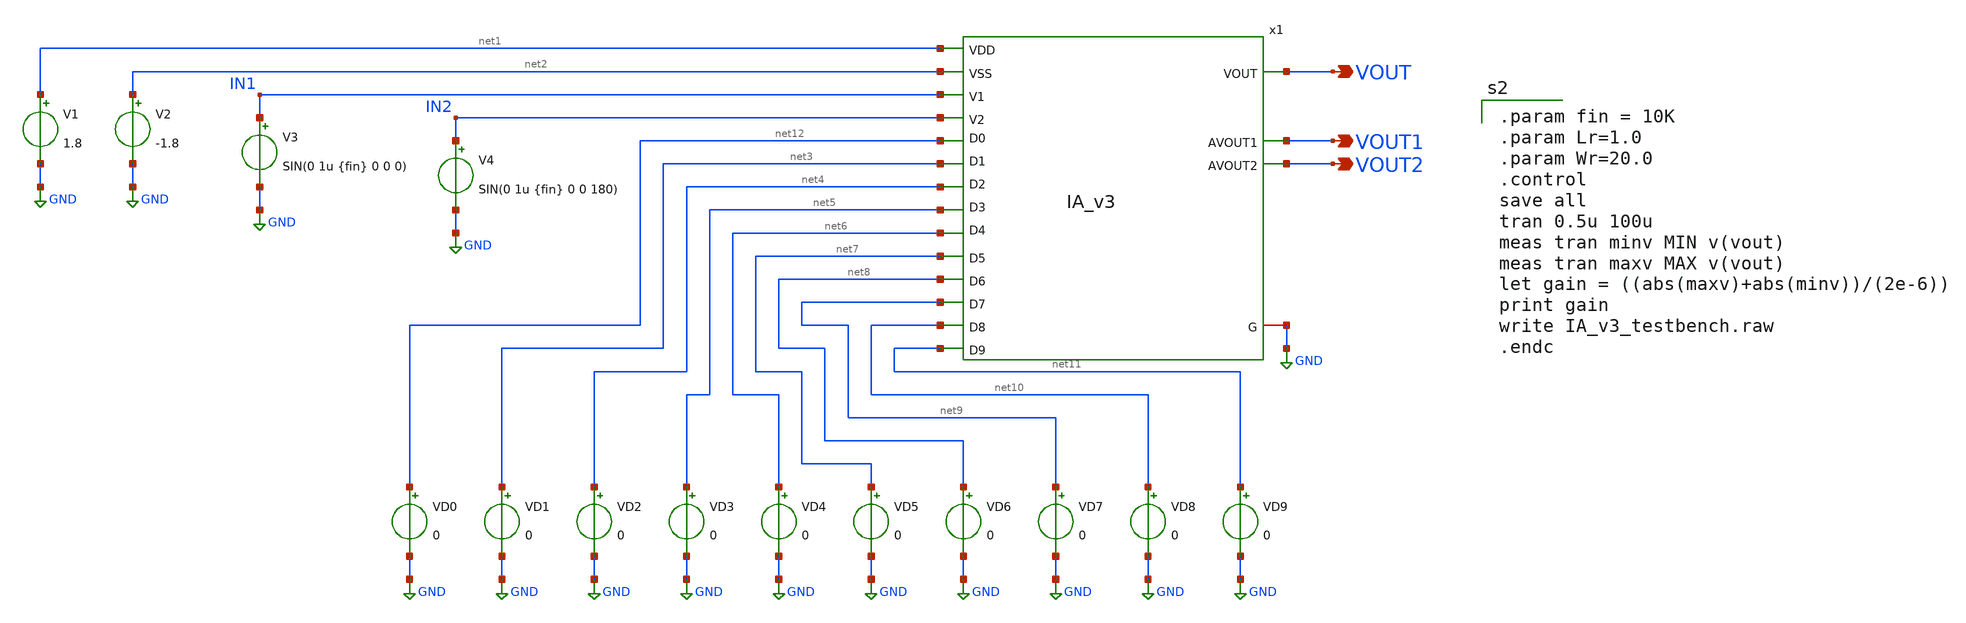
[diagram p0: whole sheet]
** sch_path: xschem/IA_v3_testbench.sch
**.subckt IA_v3_testbench VOUT VOUT1 VOUT2
*.opin VOUT
*.opin VOUT1
*.opin VOUT2
V1 net1 GND 1.8
V2 net2 GND -1.8
V3 IN1 GND SIN(0 1u {fin} 0 0 0)
V4 IN2 GND SIN(0 1u {fin} 0 0 180)
VD0 net12 GND 0
VD1 net3 GND 0
VD2 net4 GND 0
VD3 net5 GND 0
VD4 net6 GND 0
VD5 net7 GND 0
VD6 net8 GND 0
VD7 net9 GND 0
VD8 net10 GND 0
VD9 net11 GND 0
x1 VOUT1 net1 net2 VOUT IN1 IN2 VOUT2 net6 net5 net4 net3 net12 GND net8 net9 net10 net7 net11 IA_v3
**** begin user architecture code

.param fin = 10K
.param Lr=1.0
.param Wr=20.0
.control
save all
tran 0.5u 100u
meas tran minv MIN v(vout)
meas tran maxv MAX v(vout)
let gain = ((abs(maxv)+abs(minv))/(2e-6))
print gain
write IA_v3_testbench.raw
.endc

.lib $::SKYWATER_MODELS/sky130.lib.spice tt
**** end user architecture code
**.ends

* expanding   symbol:  ./IA_v3.sym # of pins=18
** sym_path: xschem/IA_v3.sym
** sch_path: xschem/IA_v3.sch
.subckt IA_v3 AVOUT1 VDD VSS VOUT V1 V2 AVOUT2 D4 D3 D2 D1 D0 G D6 D7 D8 D5 D9
*.opin VOUT
*.iopin G
*.ipin VDD
*.ipin VSS
*.ipin V1
*.ipin V2
*.ipin D4
*.ipin D3
*.ipin D2
*.ipin D1
*.ipin D0
*.ipin D9
*.ipin D8
*.ipin D7
*.ipin D6
*.ipin D5
*.opin AVOUT1
*.opin AVOUT2
x4 VDD VSS V2 net3 AVOUT1 opamp
x5 VDD VSS V1 net4 AVOUT2 opamp
x6 VDD VSS net2 net1 VOUT opamp
x1 G net3 AVOUT1 D0 D1 D2 D3 D4 VDD RA_array_v2
x2 G net4 AVOUT2 D0 D1 D2 D3 D4 VDD RA_array_v2
x3 G net1 VOUT D5 D6 D7 D8 D9 VDD RA_array_v2
x7 G net2 G D5 D6 D7 D8 D9 VDD RA_array_v2
XR1 net4 net3 G sky130_fd_pr__res_high_po_0p69 L=12.22 mult=64 m=64
XR2 net1 net6 G sky130_fd_pr__res_high_po_0p69 L=12.22 mult=64 m=64
XR3 net5 net2 G sky130_fd_pr__res_high_po_0p69 L=12.22 mult=64 m=64
x8 VDD VSS AVOUT2 net5 net5 opamp
x9 VDD VSS AVOUT1 net6 net6 opamp
.ends


* expanding   symbol:  ../xschem/opamp.sym # of pins=5
** sym_path: xschem/opamp.sym
** sch_path: xschem/opamp.sch
.subckt opamp VDD VSS V1 V2 VOUT
*.ipin VSS
*.ipin VDD
*.ipin V2
*.ipin V1
*.opin VOUT
XM2 net5 V2 net1 VSS sky130_fd_pr__nfet_01v8 L=1 W=8.5 nf=1 ad='int((nf+1)/2) * W/nf * 0.29' as='int((nf+2)/2) * W/nf * 0.29'
+ pd='2*int((nf+1)/2) * (W/nf + 0.29)' ps='2*int((nf+2)/2) * (W/nf + 0.29)' nrd='0.29 / W' nrs='0.29 / W'
+ sa=0 sb=0 sd=0 mult=1 m=1
XM1 net6 net5 VDD VDD sky130_fd_pr__pfet_01v8 L=1 W=41 nf=1 ad='int((nf+1)/2) * W/nf * 0.29' as='int((nf+2)/2) * W/nf * 0.29'
+ pd='2*int((nf+1)/2) * (W/nf + 0.29)' ps='2*int((nf+2)/2) * (W/nf + 0.29)' nrd='0.29 / W' nrs='0.29 / W'
+ sa=0 sb=0 sd=0 mult=1 m=1
XM4 net6 V1 net1 VSS sky130_fd_pr__nfet_01v8 L=1 W=8.5 nf=1 ad='int((nf+1)/2) * W/nf * 0.29' as='int((nf+2)/2) * W/nf * 0.29'
+ pd='2*int((nf+1)/2) * (W/nf + 0.29)' ps='2*int((nf+2)/2) * (W/nf + 0.29)' nrd='0.29 / W' nrs='0.29 / W'
+ sa=0 sb=0 sd=0 mult=1 m=1
XM5 net1 net4 VSS VSS sky130_fd_pr__nfet_01v8 L=1 W=20 nf=1 ad='int((nf+1)/2) * W/nf * 0.29' as='int((nf+2)/2) * W/nf * 0.29'
+ pd='2*int((nf+1)/2) * (W/nf + 0.29)' ps='2*int((nf+2)/2) * (W/nf + 0.29)' nrd='0.29 / W' nrs='0.29 / W'
+ sa=0 sb=0 sd=0 mult=1 m=1
XM6 VOUT net4 VSS VSS sky130_fd_pr__nfet_01v8 L=1 W=19 nf=1 ad='int((nf+1)/2) * W/nf * 0.29' as='int((nf+2)/2) * W/nf * 0.29'
+ pd='2*int((nf+1)/2) * (W/nf + 0.29)' ps='2*int((nf+2)/2) * (W/nf + 0.29)' nrd='0.29 / W' nrs='0.29 / W'
+ sa=0 sb=0 sd=0 mult=1 m=1
XM7 net4 net4 VSS VSS sky130_fd_pr__nfet_01v8 L=1 W=20 nf=1 ad='int((nf+1)/2) * W/nf * 0.29' as='int((nf+2)/2) * W/nf * 0.29'
+ pd='2*int((nf+1)/2) * (W/nf + 0.29)' ps='2*int((nf+2)/2) * (W/nf + 0.29)' nrd='0.29 / W' nrs='0.29 / W'
+ sa=0 sb=0 sd=0 mult=1 m=1
XM3 net5 net5 VDD VDD sky130_fd_pr__pfet_01v8 L=1 W=41 nf=1 ad='int((nf+1)/2) * W/nf * 0.29' as='int((nf+2)/2) * W/nf * 0.29'
+ pd='2*int((nf+1)/2) * (W/nf + 0.29)' ps='2*int((nf+2)/2) * (W/nf + 0.29)' nrd='0.29 / W' nrs='0.29 / W'
+ sa=0 sb=0 sd=0 mult=1 m=1
XM8 VOUT net6 VDD VDD sky130_fd_pr__pfet_01v8 L=1 W=40 nf=1 ad='int((nf+1)/2) * W/nf * 0.29' as='int((nf+2)/2) * W/nf * 0.29'
+ pd='2*int((nf+1)/2) * (W/nf + 0.29)' ps='2*int((nf+2)/2) * (W/nf + 0.29)' nrd='0.29 / W' nrs='0.29 / W'
+ sa=0 sb=0 sd=0 mult=2 m=2
XR3 net2 VDD VSS sky130_fd_pr__res_high_po W=1 L=50 mult=1 m=1
XR1 net3 net2 VSS sky130_fd_pr__res_high_po W=1 L=50 mult=1 m=1
XR2 net4 net3 VSS sky130_fd_pr__res_high_po W=1 L=50 mult=1 m=1
XR4 net7 VOUT VSS sky130_fd_pr__res_high_po W=1 L=7 mult=1 m=1
XC1 net7 net6 sky130_fd_pr__cap_mim_m3_1 W=5.55 L=10 MF=20 m=20
.ends


* expanding   symbol:  ../xschem/RA_array_v2.sym # of pins=9
** sym_path: xschem/RA_array_v2.sym
** sch_path: xschem/RA_array_v2.sch
.subckt RA_array_v2 VSS R1 R2 D0 D1 D2 D3 D4 VDD
*.ipin VSS
*.iopin R2
*.ipin D0
*.ipin D1
*.ipin D2
*.ipin D3
*.ipin D4
*.iopin R1
*.ipin VDD
XM1 net7 VDD net1 VSS sky130_fd_pr__nfet_g5v0d10v5 L={Lr} W={Wr} nf=1 ad='int((nf+1)/2) * W/nf * 0.29'
+ as='int((nf+2)/2) * W/nf * 0.29' pd='2*int((nf+1)/2) * (W/nf + 0.29)' ps='2*int((nf+2)/2) * (W/nf + 0.29)'
+ nrd='0.29 / W' nrs='0.29 / W' sa=0 sb=0 sd=0 mult=1 m=1
XM2 net8 D0 net2 VSS sky130_fd_pr__nfet_g5v0d10v5 L={Lr} W={Wr} nf=1 ad='int((nf+1)/2) * W/nf * 0.29'
+ as='int((nf+2)/2) * W/nf * 0.29' pd='2*int((nf+1)/2) * (W/nf + 0.29)' ps='2*int((nf+2)/2) * (W/nf + 0.29)'
+ nrd='0.29 / W' nrs='0.29 / W' sa=0 sb=0 sd=0 mult=1 m=1
XM3 net9 D1 net3 VSS sky130_fd_pr__nfet_g5v0d10v5 L={Lr} W={Wr} nf=1 ad='int((nf+1)/2) * W/nf * 0.29'
+ as='int((nf+2)/2) * W/nf * 0.29' pd='2*int((nf+1)/2) * (W/nf + 0.29)' ps='2*int((nf+2)/2) * (W/nf + 0.29)'
+ nrd='0.29 / W' nrs='0.29 / W' sa=0 sb=0 sd=0 mult=1 m=1
XM4 net10 D2 net4 VSS sky130_fd_pr__nfet_g5v0d10v5 L={Lr} W={Wr} nf=1 ad='int((nf+1)/2) * W/nf * 0.29'
+ as='int((nf+2)/2) * W/nf * 0.29' pd='2*int((nf+1)/2) * (W/nf + 0.29)' ps='2*int((nf+2)/2) * (W/nf + 0.29)'
+ nrd='0.29 / W' nrs='0.29 / W' sa=0 sb=0 sd=0 mult=1 m=1
XM5 net11 D3 net5 VSS sky130_fd_pr__nfet_g5v0d10v5 L={Lr} W={Wr} nf=1 ad='int((nf+1)/2) * W/nf * 0.29'
+ as='int((nf+2)/2) * W/nf * 0.29' pd='2*int((nf+1)/2) * (W/nf + 0.29)' ps='2*int((nf+2)/2) * (W/nf + 0.29)'
+ nrd='0.29 / W' nrs='0.29 / W' sa=0 sb=0 sd=0 mult=1 m=1
XM6 net12 D4 net6 VSS sky130_fd_pr__nfet_g5v0d10v5 L={Lr} W={Wr} nf=1 ad='int((nf+1)/2) * W/nf * 0.29'
+ as='int((nf+2)/2) * W/nf * 0.29' pd='2*int((nf+1)/2) * (W/nf + 0.29)' ps='2*int((nf+2)/2) * (W/nf + 0.29)'
+ nrd='0.29 / W' nrs='0.29 / W' sa=0 sb=0 sd=0 mult=1 m=1
Vmeas R1 net7 0
.save i(vmeas)
Vmeas1 R1 net8 0
.save i(vmeas1)
Vmeas2 R1 net9 0
.save i(vmeas2)
Vmeas3 R1 net10 0
.save i(vmeas3)
Vmeas4 R1 net11 0
.save i(vmeas4)
Vmeas5 R1 net12 0
.save i(vmeas5)
XR64_1 net1 R2 VSS sky130_fd_pr__res_high_po_0p69 L=12.22 mult=1 m=1
XR32 net3 R2 VSS sky130_fd_pr__res_high_po_0p69 L=12.22 mult=2 m=2
XR16 net4 R2 VSS sky130_fd_pr__res_high_po_0p69 L=12.22 mult=4 m=4
XR8 net5 R2 VSS sky130_fd_pr__res_high_po_0p69 L=12.22 mult=8 m=8
XR4 net6 R2 VSS sky130_fd_pr__res_high_po_0p69 L=12.22 mult=16 m=16
XR64_2 net2 R2 VSS sky130_fd_pr__res_high_po_0p69 L=12.22 mult=1 m=1
.ends

.GLOBAL GND
.end
